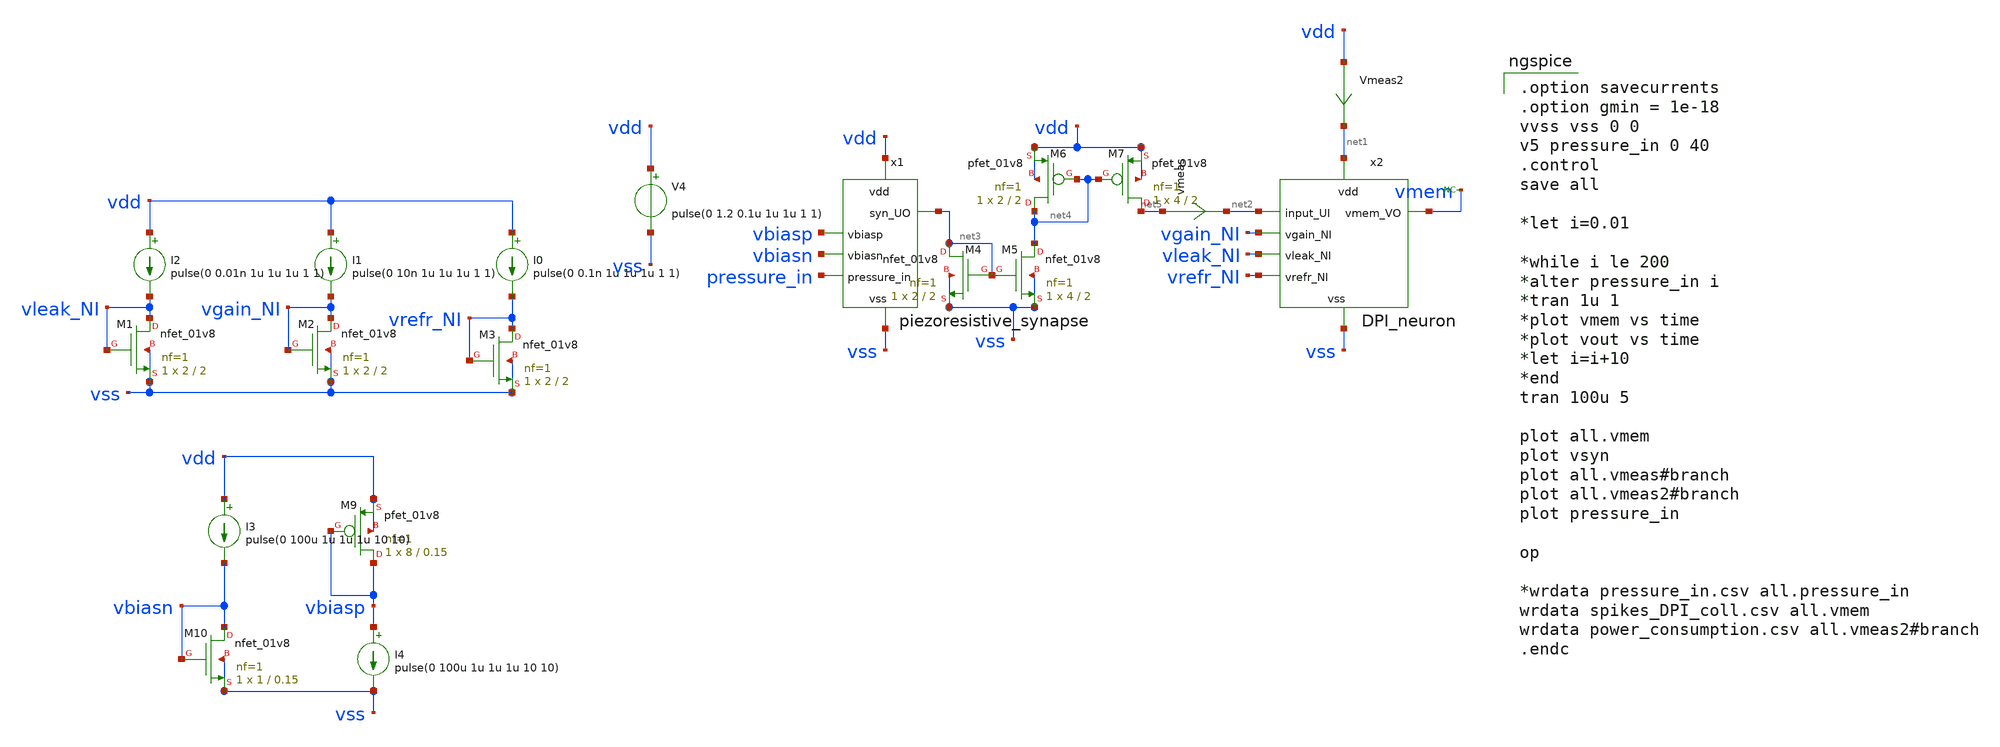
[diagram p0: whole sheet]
** sch_path: circuits/DPI_and_piezo.sch
* Copyright 2020 Stefan Frederik Schippers
* Licensed under the Apache License, Version 2.0 (the "License");
* you may not use this file except in compliance with the License.
* You may obtain a copy of the License at
* https://www.apache.org/licenses/LICENSE-2.0
* Unless required by applicable law or agreed to in writing, software
* distributed under the License is distributed on an "AS IS" BASIS,
* WITHOUT WARRANTIES OR CONDITIONS OF ANY KIND, either express or implied.
* See the License for the specific language governing permissions and
* limitations under the License.
**.subckt DPI_and_piezo
x2 net2 net1 vgain_NI vleak_NI vrefr_NI vss vmem DPI_neuron
I0 vdd vrefr_NI pulse(0 0.1n 1u 1u 1u 1 1)
I1 vdd vgain_NI pulse(0 10n 1u 1u 1u 1 1)
I2 vdd vleak_NI pulse(0 0.01n 1u 1u 1u 1 1)
XM1 vleak_NI vleak_NI vss vss sky130_fd_pr__nfet_01v8 L=2 W=2 nf=1 ad='int((nf+1)/2) * W/nf * 0.29' as='int((nf+2)/2) * W/nf * 0.29'
+ pd='2*int((nf+1)/2) * (W/nf + 0.29)' ps='2*int((nf+2)/2) * (W/nf + 0.29)' nrd='0.29 / W' nrs='0.29 / W'
+ sa=0 sb=0 sd=0 mult=1 m=1
XM2 vgain_NI vgain_NI vss vss sky130_fd_pr__nfet_01v8 L=2 W=2 nf=1 ad='int((nf+1)/2) * W/nf * 0.29' as='int((nf+2)/2) * W/nf * 0.29'
+ pd='2*int((nf+1)/2) * (W/nf + 0.29)' ps='2*int((nf+2)/2) * (W/nf + 0.29)' nrd='0.29 / W' nrs='0.29 / W'
+ sa=0 sb=0 sd=0 mult=1 m=1
XM3 vrefr_NI vrefr_NI vss vss sky130_fd_pr__nfet_01v8 L=2 W=2 nf=1 ad='int((nf+1)/2) * W/nf * 0.29' as='int((nf+2)/2) * W/nf * 0.29'
+ pd='2*int((nf+1)/2) * (W/nf + 0.29)' ps='2*int((nf+2)/2) * (W/nf + 0.29)' nrd='0.29 / W' nrs='0.29 / W'
+ sa=0 sb=0 sd=0 mult=1 m=1
V4 vdd vss pulse(0 1.2 0.1u 1u 1u 1 1)
x1 vdd vbiasp vbiasn pressure_in vss net3 piezoresistive_synapse
vmeas net5 net2 0
.save i(vmeas)
* noconn vmem
XM9 vbiasp vbiasp vdd vdd sky130_fd_pr__pfet_01v8 L=0.15 W=8 nf=1 ad='int((nf+1)/2) * W/nf * 0.29' as='int((nf+2)/2) * W/nf * 0.29'
+ pd='2*int((nf+1)/2) * (W/nf + 0.29)' ps='2*int((nf+2)/2) * (W/nf + 0.29)' nrd='0.29 / W' nrs='0.29 / W'
+ sa=0 sb=0 sd=0 mult=1 m=1
XM10 vbiasn vbiasn vss vss sky130_fd_pr__nfet_01v8 L=0.15 W=1 nf=1 ad='int((nf+1)/2) * W/nf * 0.29' as='int((nf+2)/2) * W/nf * 0.29'
+ pd='2*int((nf+1)/2) * (W/nf + 0.29)' ps='2*int((nf+2)/2) * (W/nf + 0.29)' nrd='0.29 / W' nrs='0.29 / W'
+ sa=0 sb=0 sd=0 mult=1 m=1
I3 vdd vbiasn pulse(0 100u 1u 1u 1u 10 10)
I4 vbiasp vss pulse(0 100u 1u 1u 1u 10 10)
XM4 net3 net3 vss vss sky130_fd_pr__nfet_01v8 L=2 W=2 nf=1 ad='int((nf+1)/2) * W/nf * 0.29' as='int((nf+2)/2) * W/nf * 0.29'
+ pd='2*int((nf+1)/2) * (W/nf + 0.29)' ps='2*int((nf+2)/2) * (W/nf + 0.29)' nrd='0.29 / W' nrs='0.29 / W'
+ sa=0 sb=0 sd=0 mult=1 m=1
XM5 net4 net3 vss vss sky130_fd_pr__nfet_01v8 L=2 W=4 nf=1 ad='int((nf+1)/2) * W/nf * 0.29' as='int((nf+2)/2) * W/nf * 0.29'
+ pd='2*int((nf+1)/2) * (W/nf + 0.29)' ps='2*int((nf+2)/2) * (W/nf + 0.29)' nrd='0.29 / W' nrs='0.29 / W'
+ sa=0 sb=0 sd=0 mult=1 m=1
XM6 net4 net4 vdd vdd sky130_fd_pr__pfet_01v8 L=2 W=2 nf=1 ad='int((nf+1)/2) * W/nf * 0.29' as='int((nf+2)/2) * W/nf * 0.29'
+ pd='2*int((nf+1)/2) * (W/nf + 0.29)' ps='2*int((nf+2)/2) * (W/nf + 0.29)' nrd='0.29 / W' nrs='0.29 / W'
+ sa=0 sb=0 sd=0 mult=1 m=1
XM7 net5 net4 vdd vdd sky130_fd_pr__pfet_01v8 L=2 W=4 nf=1 ad='int((nf+1)/2) * W/nf * 0.29' as='int((nf+2)/2) * W/nf * 0.29'
+ pd='2*int((nf+1)/2) * (W/nf + 0.29)' ps='2*int((nf+2)/2) * (W/nf + 0.29)' nrd='0.29 / W' nrs='0.29 / W'
+ sa=0 sb=0 sd=0 mult=1 m=1
Vmeas2 vdd net1 0
.save i(vmeas2)
**** begin user architecture code

.option savecurrents
.option gmin = 1e-18
vvss vss 0 0
v5 pressure_in 0 40
.control
save all

*let i=0.01

*while i le 200
*alter pressure_in i
*tran 1u 1
*plot vmem vs time
*plot vout vs time
*let i=i+10
*end
tran 100u 5

plot all.vmem
plot vsyn
plot all.vmeas#branch
plot all.vmeas2#branch
plot pressure_in

op

*wrdata pressure_in.csv all.pressure_in
wrdata spikes_DPI_coll.csv all.vmem
wrdata power_consumption.csv all.vmeas2#branch
.endc


 .lib $::SKYWATER_MODELS/models/sky130.lib.spice tt

.param mc_mm_switch=0
.param mc_pr_switch=1


**** end user architecture code
**.ends
.end
